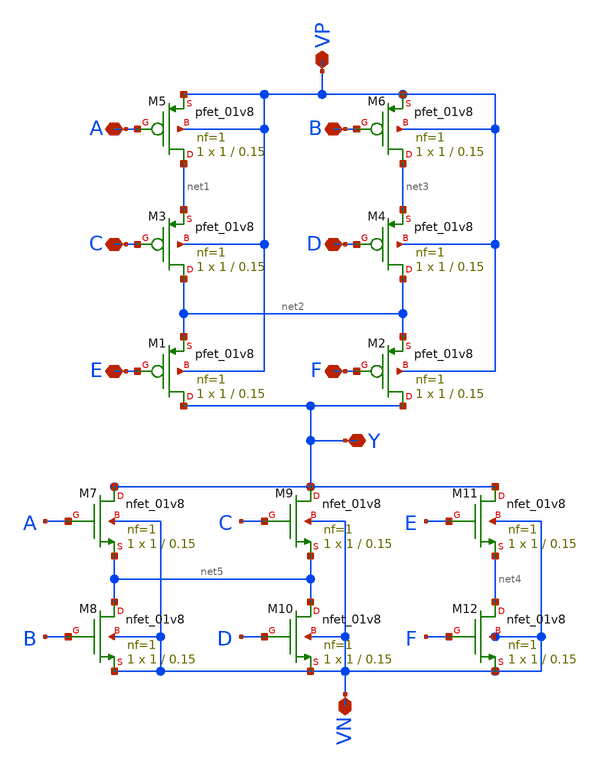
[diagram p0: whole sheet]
** sch_path: week 1/sim/3/FN.sch
**.subckt FN B A C E F D Y VP VN
*.iopin B
*.iopin A
*.iopin C
*.iopin E
*.iopin F
*.iopin D
*.iopin Y
*.iopin VP
*.iopin VN
XM1 Y E net2 VP sky130_fd_pr__pfet_01v8 L=0.15 W=1 nf=1 ad='int((nf+1)/2) * W/nf * 0.29' as='int((nf+2)/2) * W/nf * 0.29'
+ pd='2*int((nf+1)/2) * (W/nf + 0.29)' ps='2*int((nf+2)/2) * (W/nf + 0.29)' nrd='0.29 / W' nrs='0.29 / W'
+ sa=0 sb=0 sd=0 mult=1 m=1
XM2 Y F net2 VP sky130_fd_pr__pfet_01v8 L=0.15 W=1 nf=1 ad='int((nf+1)/2) * W/nf * 0.29' as='int((nf+2)/2) * W/nf * 0.29'
+ pd='2*int((nf+1)/2) * (W/nf + 0.29)' ps='2*int((nf+2)/2) * (W/nf + 0.29)' nrd='0.29 / W' nrs='0.29 / W'
+ sa=0 sb=0 sd=0 mult=1 m=1
XM3 net2 C net1 VP sky130_fd_pr__pfet_01v8 L=0.15 W=1 nf=1 ad='int((nf+1)/2) * W/nf * 0.29' as='int((nf+2)/2) * W/nf * 0.29'
+ pd='2*int((nf+1)/2) * (W/nf + 0.29)' ps='2*int((nf+2)/2) * (W/nf + 0.29)' nrd='0.29 / W' nrs='0.29 / W'
+ sa=0 sb=0 sd=0 mult=1 m=1
XM4 net2 D net3 VP sky130_fd_pr__pfet_01v8 L=0.15 W=1 nf=1 ad='int((nf+1)/2) * W/nf * 0.29' as='int((nf+2)/2) * W/nf * 0.29'
+ pd='2*int((nf+1)/2) * (W/nf + 0.29)' ps='2*int((nf+2)/2) * (W/nf + 0.29)' nrd='0.29 / W' nrs='0.29 / W'
+ sa=0 sb=0 sd=0 mult=1 m=1
XM5 net1 A VP VP sky130_fd_pr__pfet_01v8 L=0.15 W=1 nf=1 ad='int((nf+1)/2) * W/nf * 0.29' as='int((nf+2)/2) * W/nf * 0.29'
+ pd='2*int((nf+1)/2) * (W/nf + 0.29)' ps='2*int((nf+2)/2) * (W/nf + 0.29)' nrd='0.29 / W' nrs='0.29 / W'
+ sa=0 sb=0 sd=0 mult=1 m=1
XM6 net3 B VP VP sky130_fd_pr__pfet_01v8 L=0.15 W=1 nf=1 ad='int((nf+1)/2) * W/nf * 0.29' as='int((nf+2)/2) * W/nf * 0.29'
+ pd='2*int((nf+1)/2) * (W/nf + 0.29)' ps='2*int((nf+2)/2) * (W/nf + 0.29)' nrd='0.29 / W' nrs='0.29 / W'
+ sa=0 sb=0 sd=0 mult=1 m=1
XM7 Y A net5 VN sky130_fd_pr__nfet_01v8 L=0.15 W=1 nf=1 ad='int((nf+1)/2) * W/nf * 0.29' as='int((nf+2)/2) * W/nf * 0.29'
+ pd='2*int((nf+1)/2) * (W/nf + 0.29)' ps='2*int((nf+2)/2) * (W/nf + 0.29)' nrd='0.29 / W' nrs='0.29 / W'
+ sa=0 sb=0 sd=0 mult=1 m=1
XM8 net5 B VN VN sky130_fd_pr__nfet_01v8 L=0.15 W=1 nf=1 ad='int((nf+1)/2) * W/nf * 0.29' as='int((nf+2)/2) * W/nf * 0.29'
+ pd='2*int((nf+1)/2) * (W/nf + 0.29)' ps='2*int((nf+2)/2) * (W/nf + 0.29)' nrd='0.29 / W' nrs='0.29 / W'
+ sa=0 sb=0 sd=0 mult=1 m=1
XM9 Y C net5 VN sky130_fd_pr__nfet_01v8 L=0.15 W=1 nf=1 ad='int((nf+1)/2) * W/nf * 0.29' as='int((nf+2)/2) * W/nf * 0.29'
+ pd='2*int((nf+1)/2) * (W/nf + 0.29)' ps='2*int((nf+2)/2) * (W/nf + 0.29)' nrd='0.29 / W' nrs='0.29 / W'
+ sa=0 sb=0 sd=0 mult=1 m=1
XM10 net5 D VN VN sky130_fd_pr__nfet_01v8 L=0.15 W=1 nf=1 ad='int((nf+1)/2) * W/nf * 0.29' as='int((nf+2)/2) * W/nf * 0.29'
+ pd='2*int((nf+1)/2) * (W/nf + 0.29)' ps='2*int((nf+2)/2) * (W/nf + 0.29)' nrd='0.29 / W' nrs='0.29 / W'
+ sa=0 sb=0 sd=0 mult=1 m=1
XM11 Y E net4 VN sky130_fd_pr__nfet_01v8 L=0.15 W=1 nf=1 ad='int((nf+1)/2) * W/nf * 0.29' as='int((nf+2)/2) * W/nf * 0.29'
+ pd='2*int((nf+1)/2) * (W/nf + 0.29)' ps='2*int((nf+2)/2) * (W/nf + 0.29)' nrd='0.29 / W' nrs='0.29 / W'
+ sa=0 sb=0 sd=0 mult=1 m=1
XM12 net4 F VN VN sky130_fd_pr__nfet_01v8 L=0.15 W=1 nf=1 ad='int((nf+1)/2) * W/nf * 0.29' as='int((nf+2)/2) * W/nf * 0.29'
+ pd='2*int((nf+1)/2) * (W/nf + 0.29)' ps='2*int((nf+2)/2) * (W/nf + 0.29)' nrd='0.29 / W' nrs='0.29 / W'
+ sa=0 sb=0 sd=0 mult=1 m=1
**.ends
.end
